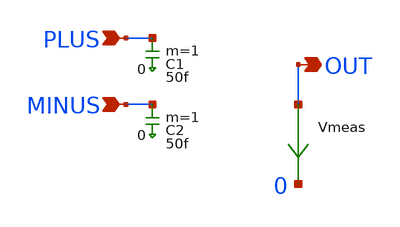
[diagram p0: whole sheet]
** sch_path: xschem_library/inst_sch_select/comp_65nm_parax.sch
**.subckt comp_65nm_parax OUT MINUS PLUS
*.opin OUT
*.ipin MINUS
*.ipin PLUS
C1 PLUS 0 50f m=1
C2 MINUS 0 50f m=1
Vmeas OUT 0 0
.save i(vmeas)
**.ends
.end
